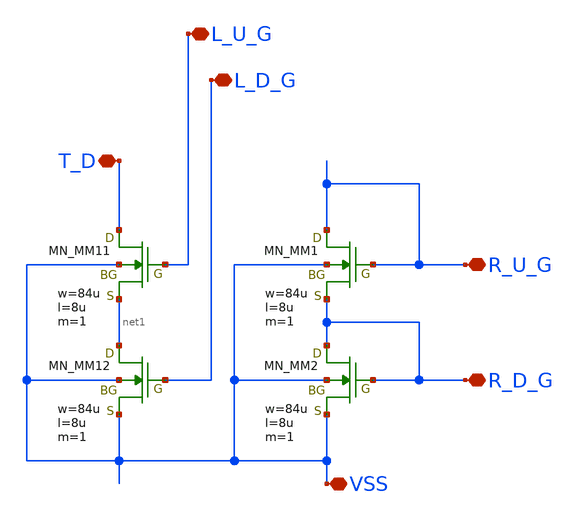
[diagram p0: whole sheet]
** sch_path: member_project/AM_Radio/noritsuna/xschem/CM_NMOS_base.sch
**.subckt CM_NMOS_base VSS R_D_G R_U_G L_U_G L_D_G T_D
*.iopin VSS
*.iopin R_D_G
*.iopin R_U_G
*.iopin L_U_G
*.iopin L_D_G
*.iopin T_D
MM1 R_U_G R_U_G R_D_G VSS NMOS w=84u l=8u as=0 ad=0 ps=0 pd=0 nrd=0 nrs=0 m=1
MM2 R_D_G R_D_G VSS VSS NMOS w=84u l=8u as=0 ad=0 ps=0 pd=0 nrd=0 nrs=0 m=1
MM11 T_D L_U_G net1 VSS NMOS w=84u l=8u as=0 ad=0 ps=0 pd=0 nrd=0 nrs=0 m=1
MM12 net1 L_D_G VSS VSS NMOS w=84u l=8u as=0 ad=0 ps=0 pd=0 nrd=0 nrs=0 m=1
**.ends
.end
